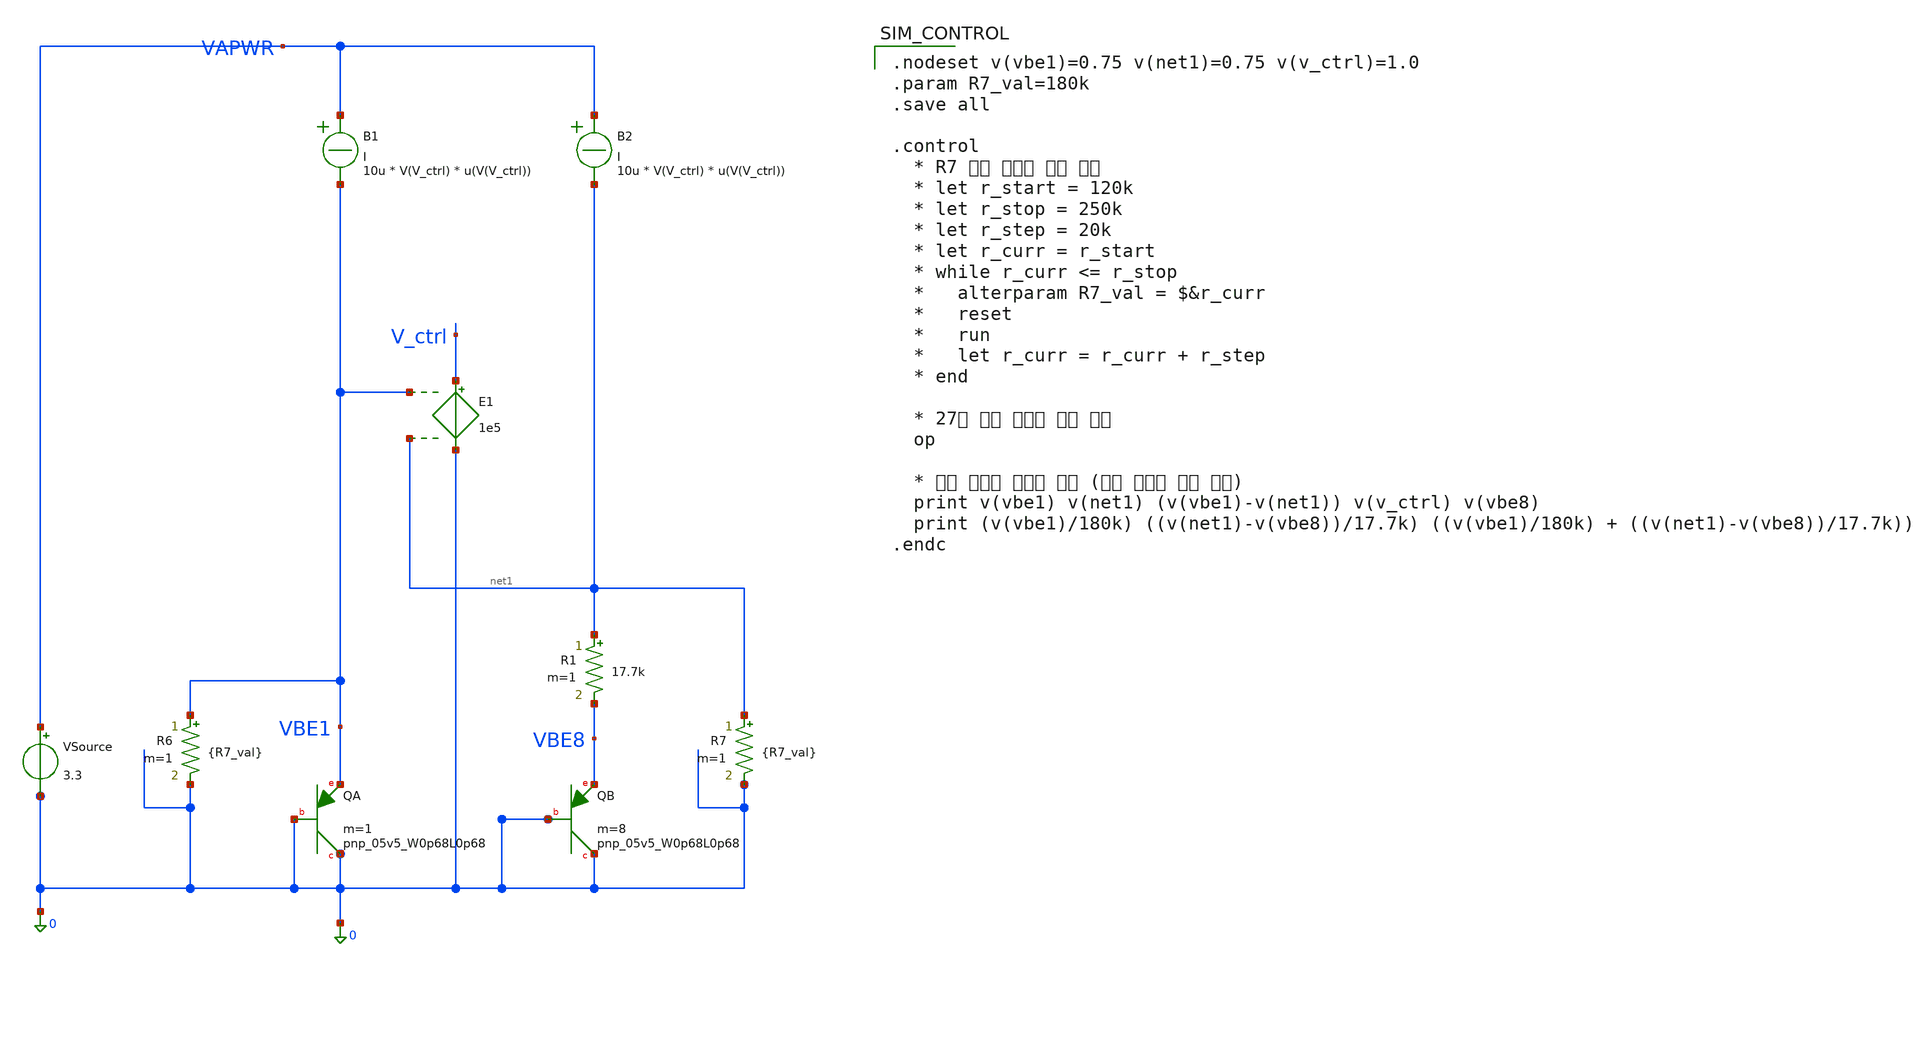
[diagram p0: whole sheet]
** sch_path: designs/bgr_ldo/milestones/01_selfbias_op_verified/bgr_core_tb.sch
**.subckt bgr_core_tb
XQA 0 0 VBE1 sky130_fd_pr__pnp_05v5_W0p68L0p68 m=1
VSource VAPWR 0 3.3
XQB 0 0 VBE8 sky130_fd_pr__pnp_05v5_W0p68L0p68 m=8
R1 net1 VBE8 17.7k m=1
R7 net1 0 {R7_val} m=1
R6 VBE1 0 {R7_val} m=1
E1 V_ctrl 0 VBE1 net1 1e5
B1 VAPWR VBE1 I = 10u * V(V_ctrl) * u(V(V_ctrl))
B2 VAPWR net1 I = 10u * V(V_ctrl) * u(V(V_ctrl))
**** begin user architecture code

.nodeset v(vbe1)=0.75 v(net1)=0.75 v(v_ctrl)=1.0
.param R7_val=180k
.save all

.control
  * R7 스윕 루프는 주석 처리
  * let r_start = 120k
  * let r_stop = 250k
  * let r_step = 20k
  * let r_curr = r_start
  * while r_curr <= r_stop
  *   alterparam R7_val = $&r_curr
  *   reset
  *   run
  *   let r_curr = r_curr + r_step
  * end

  * 27도 단일 동작점 해석 실행
  op

  * 결과 보고용 데이터 출력 (에러 방지용 수식 적용)
  print v(vbe1) v(net1) (v(vbe1)-v(net1)) v(v_ctrl) v(vbe8)
  print (v(vbe1)/180k) ((v(net1)-v(vbe8))/17.7k) ((v(vbe1)/180k) + ((v(net1)-v(vbe8))/17.7k))
.endc


** opencircuitdesign pdks install
.lib $::SKYWATER_MODELS/sky130.lib.spice tt

**** end user architecture code
**.ends
.end
